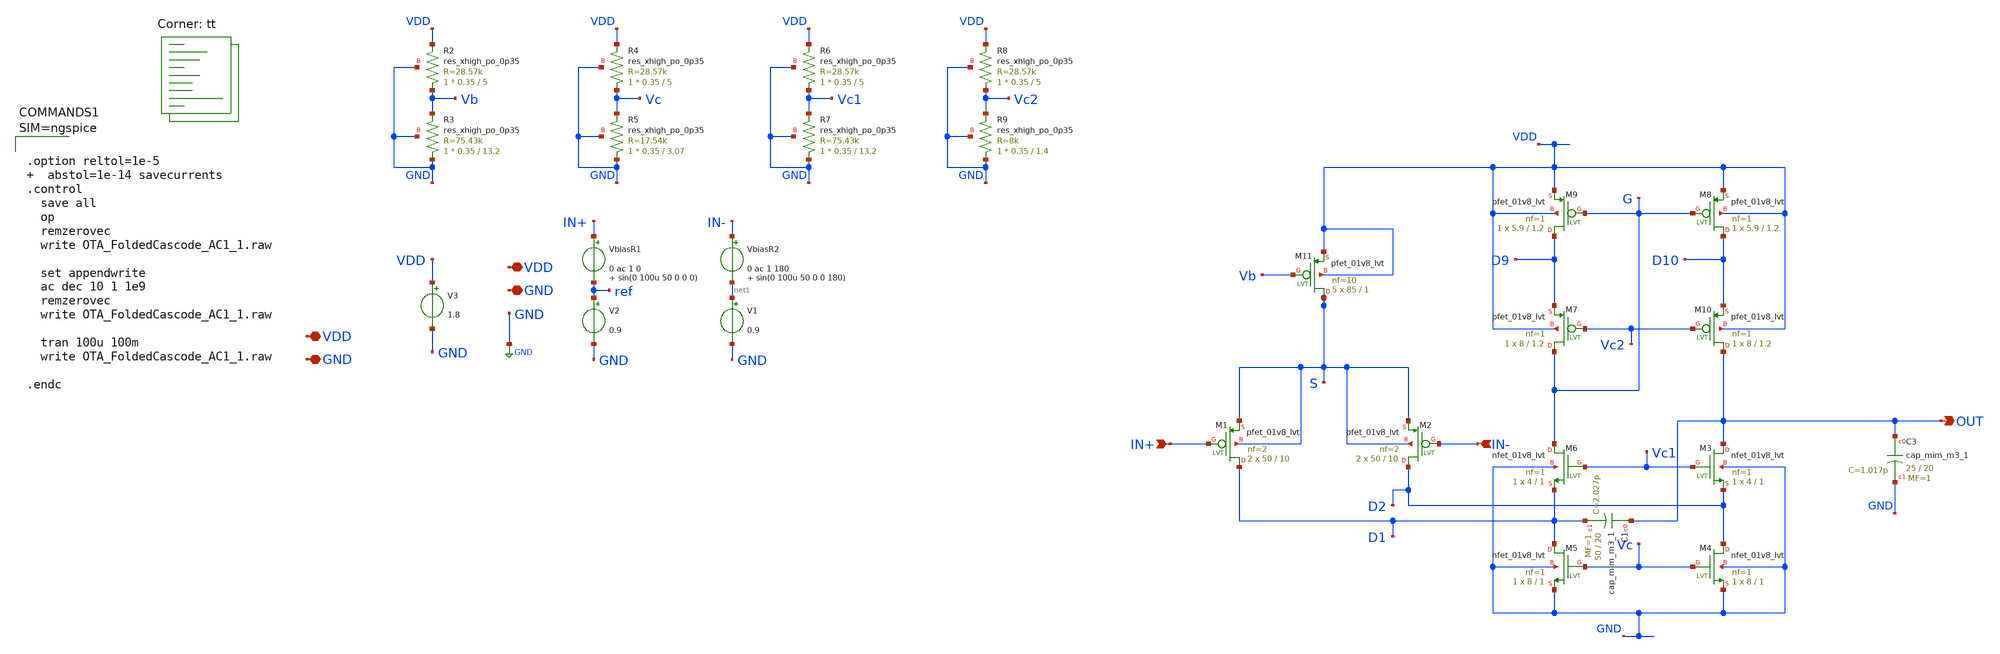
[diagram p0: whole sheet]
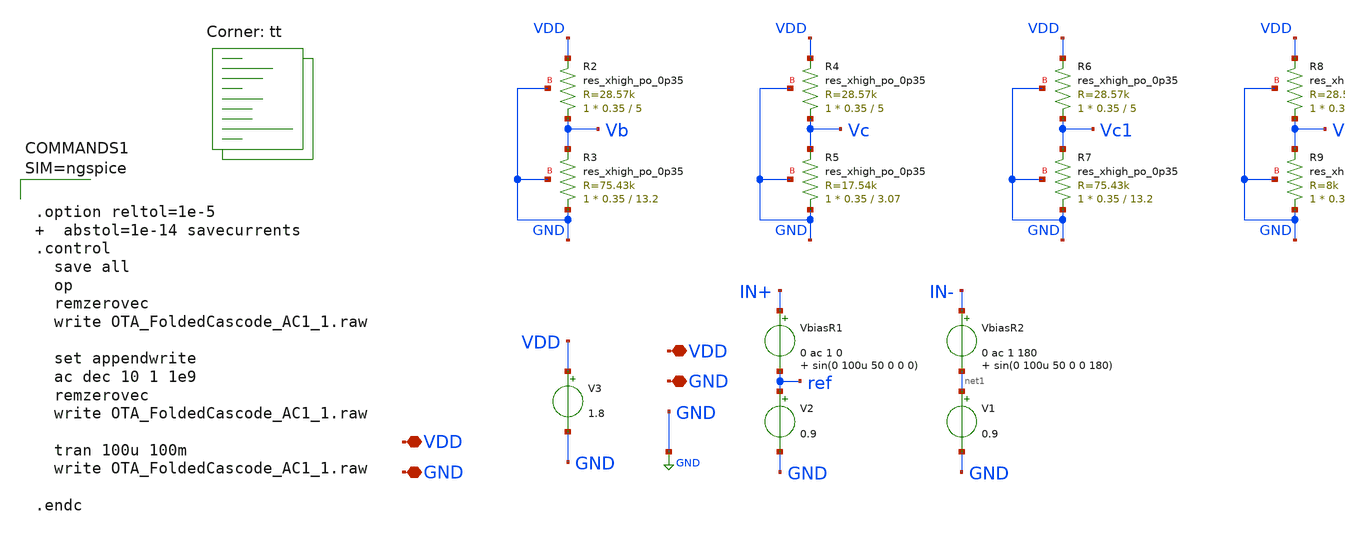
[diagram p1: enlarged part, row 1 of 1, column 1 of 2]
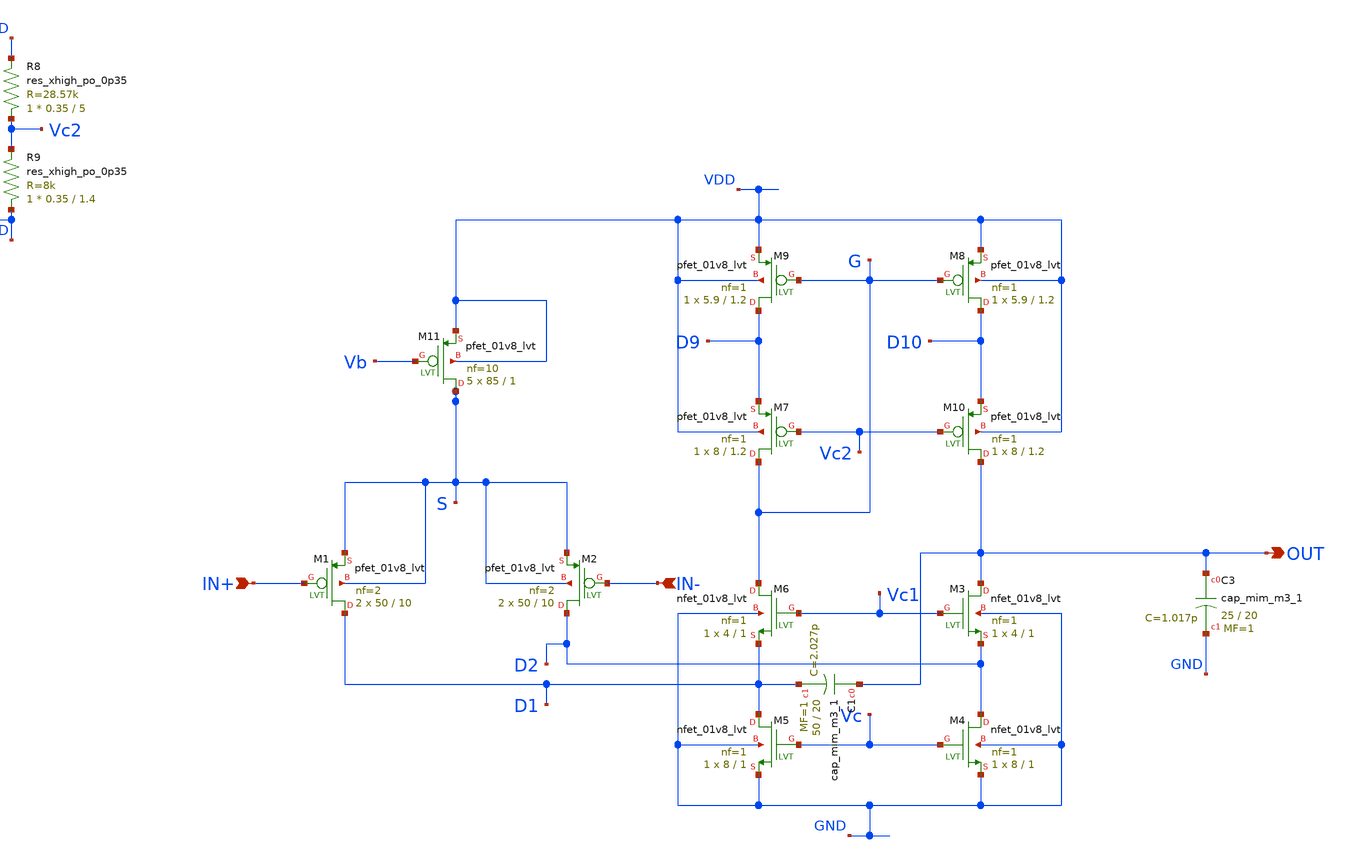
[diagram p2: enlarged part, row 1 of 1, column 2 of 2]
** sch_path: xschem/OTA_FoldedCascode_AC1_1.sch
**.subckt OTA_FoldedCascode_AC1_1 VDD GND OUT VDD GND IN+ IN-
*.iopin VDD
*.iopin GND
*.opin OUT
*.iopin VDD
*.iopin GND
*.ipin IN+
*.ipin IN-
VbiasR1 IN+ ref 0 ac 1 0 sin(0 100u 50 0 0 0)
V2 ref GND 0.9
XC3 OUT GND sky130_fd_pr__cap_mim_m3_1 W=25 L=20 MF=1 m=1
V3 VDD GND 1.8
XM11 S Vb VDD VDD sky130_fd_pr__pfet_01v8_lvt L=1 W=85 nf=10 ad='int((nf+1)/2) * W/nf * 0.29' as='int((nf+2)/2) * W/nf * 0.29'
+ pd='2*int((nf+1)/2) * (W/nf + 0.29)' ps='2*int((nf+2)/2) * (W/nf + 0.29)' nrd='0.29 / W' nrs='0.29 / W'
+ sa=0 sb=0 sd=0 mult=5 m=5
XM1 D1 IN+ S S sky130_fd_pr__pfet_01v8_lvt L=10 W=50 nf=2 ad='int((nf+1)/2) * W/nf * 0.29' as='int((nf+2)/2) * W/nf * 0.29'
+ pd='2*int((nf+1)/2) * (W/nf + 0.29)' ps='2*int((nf+2)/2) * (W/nf + 0.29)' nrd='0.29 / W' nrs='0.29 / W'
+ sa=0 sb=0 sd=0 mult=2 m=2
XM2 D2 IN- S S sky130_fd_pr__pfet_01v8_lvt L=10 W=50 nf=2 ad='int((nf+1)/2) * W/nf * 0.29' as='int((nf+2)/2) * W/nf * 0.29'
+ pd='2*int((nf+1)/2) * (W/nf + 0.29)' ps='2*int((nf+2)/2) * (W/nf + 0.29)' nrd='0.29 / W' nrs='0.29 / W'
+ sa=0 sb=0 sd=0 mult=2 m=2
XM3 OUT Vc1 D2 GND sky130_fd_pr__nfet_01v8_lvt L=1 W=4 nf=1 ad='int((nf+1)/2) * W/nf * 0.29' as='int((nf+2)/2) * W/nf * 0.29'
+ pd='2*int((nf+1)/2) * (W/nf + 0.29)' ps='2*int((nf+2)/2) * (W/nf + 0.29)' nrd='0.29 / W' nrs='0.29 / W'
+ sa=0 sb=0 sd=0 mult=1 m=1
XM4 D2 Vc GND GND sky130_fd_pr__nfet_01v8_lvt L=1 W=8 nf=1 ad='int((nf+1)/2) * W/nf * 0.29' as='int((nf+2)/2) * W/nf * 0.29'
+ pd='2*int((nf+1)/2) * (W/nf + 0.29)' ps='2*int((nf+2)/2) * (W/nf + 0.29)' nrd='0.29 / W' nrs='0.29 / W'
+ sa=0 sb=0 sd=0 mult=1 m=1
XM5 D1 Vc GND GND sky130_fd_pr__nfet_01v8_lvt L=1 W=8 nf=1 ad='int((nf+1)/2) * W/nf * 0.29' as='int((nf+2)/2) * W/nf * 0.29'
+ pd='2*int((nf+1)/2) * (W/nf + 0.29)' ps='2*int((nf+2)/2) * (W/nf + 0.29)' nrd='0.29 / W' nrs='0.29 / W'
+ sa=0 sb=0 sd=0 mult=1 m=1
XM6 G Vc1 D1 GND sky130_fd_pr__nfet_01v8_lvt L=1 W=4 nf=1 ad='int((nf+1)/2) * W/nf * 0.29' as='int((nf+2)/2) * W/nf * 0.29'
+ pd='2*int((nf+1)/2) * (W/nf + 0.29)' ps='2*int((nf+2)/2) * (W/nf + 0.29)' nrd='0.29 / W' nrs='0.29 / W'
+ sa=0 sb=0 sd=0 mult=1 m=1
XR2 Vb VDD GND sky130_fd_pr__res_xhigh_po_0p35 L=5 mult=1 m=1
XR3 GND Vb GND sky130_fd_pr__res_xhigh_po_0p35 L=13.2 mult=1 m=1
XR4 Vc VDD GND sky130_fd_pr__res_xhigh_po_0p35 L=5 mult=1 m=1
XR5 GND Vc GND sky130_fd_pr__res_xhigh_po_0p35 L=3.07 mult=1 m=1
XR6 Vc1 VDD GND sky130_fd_pr__res_xhigh_po_0p35 L=5 mult=1 m=1
XR7 GND Vc1 GND sky130_fd_pr__res_xhigh_po_0p35 L=13.2 mult=1 m=1
XR8 Vc2 VDD GND sky130_fd_pr__res_xhigh_po_0p35 L=5 mult=1 m=1
XR9 GND Vc2 GND sky130_fd_pr__res_xhigh_po_0p35 L=1.4 mult=1 m=1
XM7 G Vc2 D9 VDD sky130_fd_pr__pfet_01v8_lvt L=1.2 W=8 nf=1 ad='int((nf+1)/2) * W/nf * 0.29' as='int((nf+2)/2) * W/nf * 0.29'
+ pd='2*int((nf+1)/2) * (W/nf + 0.29)' ps='2*int((nf+2)/2) * (W/nf + 0.29)' nrd='0.29 / W' nrs='0.29 / W'
+ sa=0 sb=0 sd=0 mult=1 m=1
XM9 D9 G VDD VDD sky130_fd_pr__pfet_01v8_lvt L=1.2 W=5.9 nf=1 ad='int((nf+1)/2) * W/nf * 0.29' as='int((nf+2)/2) * W/nf * 0.29'
+ pd='2*int((nf+1)/2) * (W/nf + 0.29)' ps='2*int((nf+2)/2) * (W/nf + 0.29)' nrd='0.29 / W' nrs='0.29 / W'
+ sa=0 sb=0 sd=0 mult=1 m=1
XM8 D10 G VDD VDD sky130_fd_pr__pfet_01v8_lvt L=1.2 W=5.9 nf=1 ad='int((nf+1)/2) * W/nf * 0.29' as='int((nf+2)/2) * W/nf * 0.29'
+ pd='2*int((nf+1)/2) * (W/nf + 0.29)' ps='2*int((nf+2)/2) * (W/nf + 0.29)' nrd='0.29 / W' nrs='0.29 / W'
+ sa=0 sb=0 sd=0 mult=1 m=1
XM10 OUT Vc2 D10 VDD sky130_fd_pr__pfet_01v8_lvt L=1.2 W=8 nf=1 ad='int((nf+1)/2) * W/nf * 0.29' as='int((nf+2)/2) * W/nf * 0.29'
+ pd='2*int((nf+1)/2) * (W/nf + 0.29)' ps='2*int((nf+2)/2) * (W/nf + 0.29)' nrd='0.29 / W' nrs='0.29 / W'
+ sa=0 sb=0 sd=0 mult=1 m=1
XC1 OUT D1 sky130_fd_pr__cap_mim_m3_1 W=50 L=20 MF=1 m=1
VbiasR2 IN- net1 0 ac 1 180 sin(0 100u 50 0 0 180)
V1 net1 GND 0.9
**** begin user architecture code



.option reltol=1e-5   abstol=1e-14 savecurrents
.control
  save all
  op
  remzerovec
  write OTA_FoldedCascode_AC1_1.raw

  set appendwrite
  ac dec 10 1 1e9
  remzerovec
  write OTA_FoldedCascode_AC1_1.raw

  tran 100u 100m
  write OTA_FoldedCascode_AC1_1.raw

.endc



.lib $::SKYWATER_MODELS/sky130.lib.spice tt
**** end user architecture code
**.ends
.GLOBAL GND
.end
